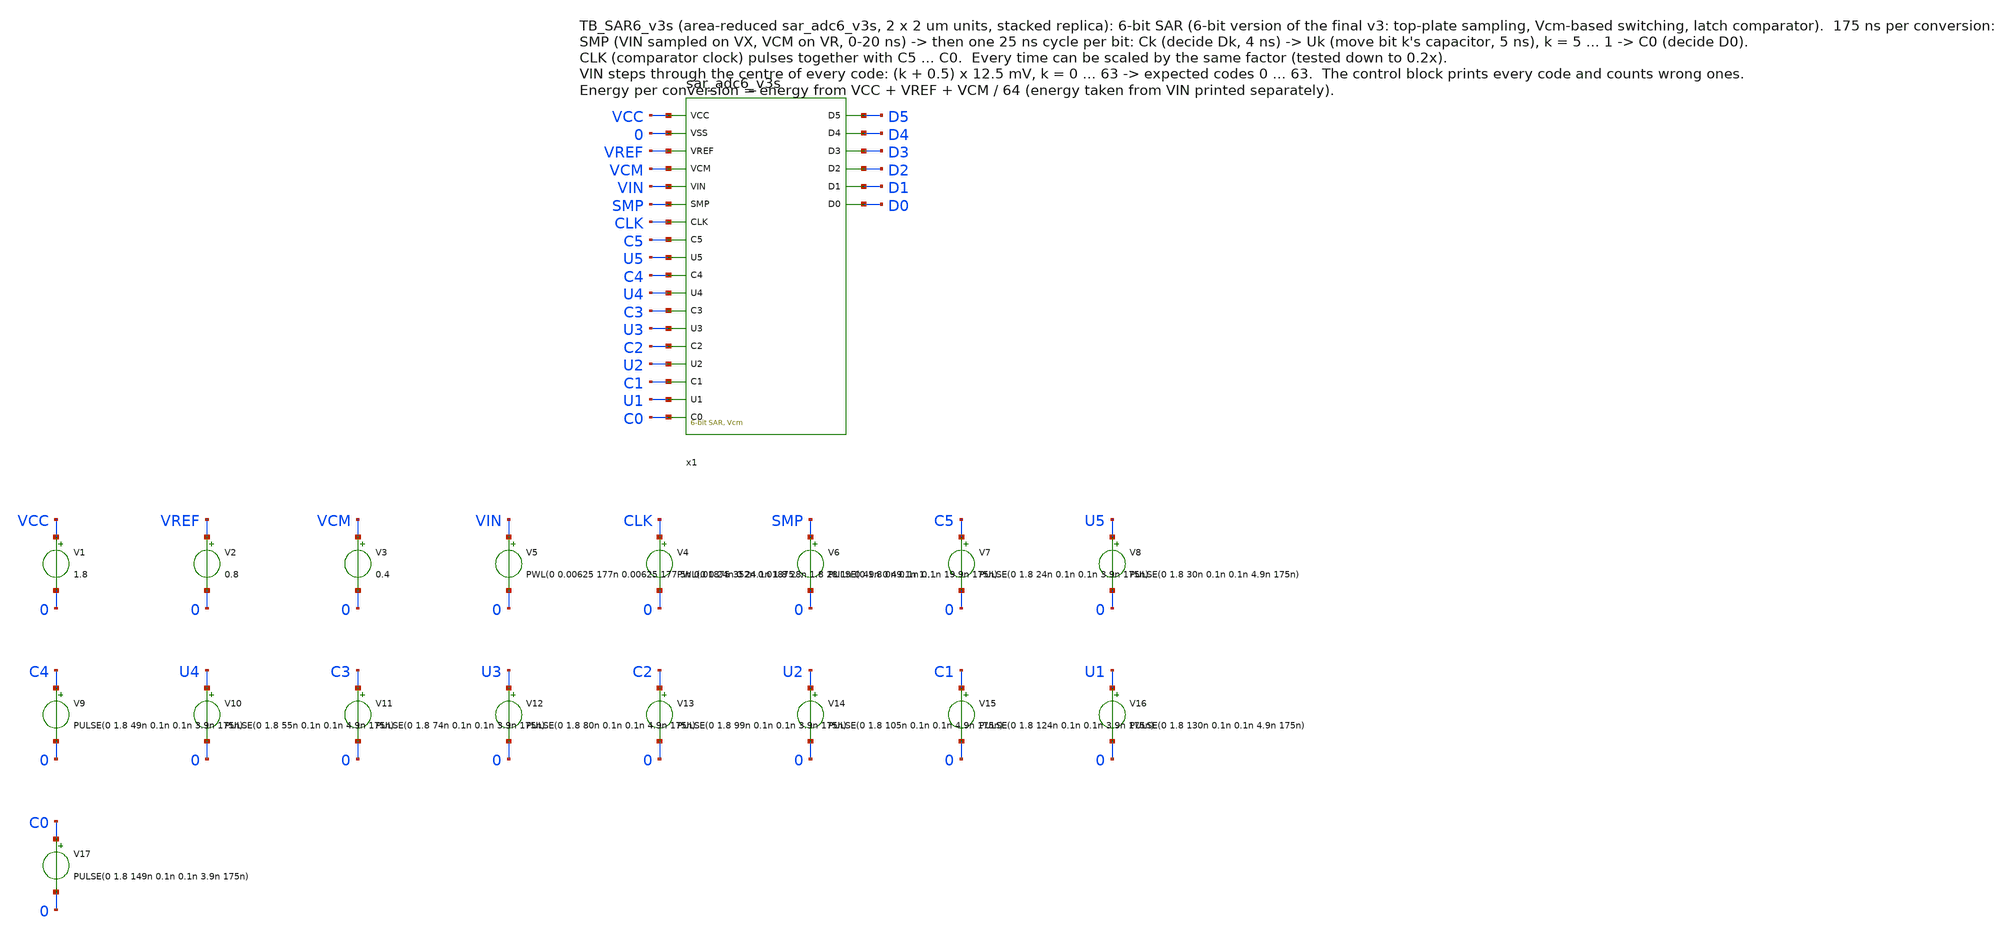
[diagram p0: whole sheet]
** sch_path: SAR_improved/TB_SAR6_v3s.sch
**.subckt TB_SAR6_v3s
x1 VCC 0 VREF VCM VIN SMP CLK C5 U5 C4 U4 C3 U3 C2 U2 C1 U1 C0 D5 D4 D3 D2 D1 D0 sar_adc6_v3s
V1 VCC 0 1.8
V2 VREF 0 0.8
V3 VCM 0 0.4
V5 VIN 0 PWL(0 0.00625 177n 0.00625 177.5n 0.01875 352n 0.01875 352.5n 0.03125 527n 0.03125 527.5n
+ 0.04375 702n 0.04375 702.5n 0.05625 877n 0.05625 877.5n 0.06875 1052n 0.06875 1052.5n 0.08125 1227n 0.08125
+ 1227.5n 0.09375 1402n 0.09375 1402.5n 0.10625 1577n 0.10625 1577.5n 0.11875 1752n 0.11875 1752.5n 0.13125
+ 1927n 0.13125 1927.5n 0.14375 2102n 0.14375 2102.5n 0.15625 2277n 0.15625 2277.5n 0.16875 2452n 0.16875
+ 2452.5n 0.18125 2627n 0.18125 2627.5n 0.19375 2802n 0.19375 2802.5n 0.20625 2977n 0.20625 2977.5n 0.21875
+ 3152n 0.21875 3152.5n 0.23125 3327n 0.23125 3327.5n 0.24375 3502n 0.24375 3502.5n 0.25625 3677n 0.25625
+ 3677.5n 0.26875 3852n 0.26875 3852.5n 0.28125 4027n 0.28125 4027.5n 0.29375 4202n 0.29375 4202.5n 0.30625
+ 4377n 0.30625 4377.5n 0.31875 4552n 0.31875 4552.5n 0.33125 4727n 0.33125 4727.5n 0.34375 4902n 0.34375
+ 4902.5n 0.35625 5077n 0.35625 5077.5n 0.36875 5252n 0.36875 5252.5n 0.38125 5427n 0.38125 5427.5n 0.39375
+ 5602n 0.39375 5602.5n 0.40625 5777n 0.40625 5777.5n 0.41875 5952n 0.41875 5952.5n 0.43125 6127n 0.43125
+ 6127.5n 0.44375 6302n 0.44375 6302.5n 0.45625 6477n 0.45625 6477.5n 0.46875 6652n 0.46875 6652.5n 0.48125
+ 6827n 0.48125 6827.5n 0.49375 7002n 0.49375 7002.5n 0.50625 7177n 0.50625 7177.5n 0.51875 7352n 0.51875
+ 7352.5n 0.53125 7527n 0.53125 7527.5n 0.54375 7702n 0.54375 7702.5n 0.55625 7877n 0.55625 7877.5n 0.56875
+ 8052n 0.56875 8052.5n 0.58125 8227n 0.58125 8227.5n 0.59375 8402n 0.59375 8402.5n 0.60625 8577n 0.60625
+ 8577.5n 0.61875 8752n 0.61875 8752.5n 0.63125 8927n 0.63125 8927.5n 0.64375 9102n 0.64375 9102.5n 0.65625
+ 9277n 0.65625 9277.5n 0.66875 9452n 0.66875 9452.5n 0.68125 9627n 0.68125 9627.5n 0.69375 9802n 0.69375
+ 9802.5n 0.70625 9977n 0.70625 9977.5n 0.71875 10152n 0.71875 10152.5n 0.73125 10327n 0.73125 10327.5n
+ 0.74375 10502n 0.74375 10502.5n 0.75625 10677n 0.75625 10677.5n 0.76875 10852n 0.76875 10852.5n 0.78125
+ 11027n 0.78125 11027.5n 0.79375)
V4 CLK 0 PWL(0 0 24n 0 24.1n 1.8 28n 1.8 28.1n 0 49n 0 49.1n 1.8 53n 1.8 53.1n 0 74n 0 74.1n 1.8 78n
+ 1.8 78.1n 0 99n 0 99.1n 1.8 103n 1.8 103.1n 0 124n 0 124.1n 1.8 128n 1.8 128.1n 0 149n 0 149.1n 1.8
+ 153n 1.8 153.1n 0 175n 0) r=0
V6 SMP 0 PULSE(0 1.8 0n 0.1n 0.1n 19.9n 175n)
V7 C5 0 PULSE(0 1.8 24n 0.1n 0.1n 3.9n 175n)
V8 U5 0 PULSE(0 1.8 30n 0.1n 0.1n 4.9n 175n)
V9 C4 0 PULSE(0 1.8 49n 0.1n 0.1n 3.9n 175n)
V10 U4 0 PULSE(0 1.8 55n 0.1n 0.1n 4.9n 175n)
V11 C3 0 PULSE(0 1.8 74n 0.1n 0.1n 3.9n 175n)
V12 U3 0 PULSE(0 1.8 80n 0.1n 0.1n 4.9n 175n)
V13 C2 0 PULSE(0 1.8 99n 0.1n 0.1n 3.9n 175n)
V14 U2 0 PULSE(0 1.8 105n 0.1n 0.1n 4.9n 175n)
V15 C1 0 PULSE(0 1.8 124n 0.1n 0.1n 3.9n 175n)
V16 U1 0 PULSE(0 1.8 130n 0.1n 0.1n 4.9n 175n)
V17 C0 0 PULSE(0 1.8 149n 0.1n 0.1n 3.9n 175n)
**** begin user architecture code

.lib /home/ttuser/pdk/sky130A/libs.tech/combined/sky130.lib.spice tt
.option method=gear reltol=1e-4
.control
save all
tran 0.05n 11200n
let code = 0*v(D0)
let code = code + 32*ceil((v(D5)-0.9)/10)
let code = code + 16*ceil((v(D4)-0.9)/10)
let code = code + 8*ceil((v(D3)-0.9)/10)
let code = code + 4*ceil((v(D2)-0.9)/10)
let code = code + 2*ceil((v(D1)-0.9)/10)
let code = code + 1*ceil((v(D0)-0.9)/10)
let nwrong = 0
let k = 0
while k < 64
  let tr = k*175e-9 + 165e-9
  meas tran ck find code at=$&tr
  print k ck
  if abs(ck - k) > 0.5
    let nwrong = nwrong + 1
  end
  let k = k + 1
end
print nwrong
let ptot = 1.8*(-i(V1)) + 0.8*(-i(V2)) + 0.4*(-i(V3))
let pin = v(VIN)*(-i(V5))
meas tran etot integ ptot from=0 to=11200n
meas tran ein integ pin from=0 to=11200n
let e_conv_pJ = etot/64*1e12
let e_from_vin_pJ = ein/64*1e12
let p_uW = etot/11200e-9*1e6
print e_conv_pJ p_uW e_from_vin_pJ
plot v(VIN) v(x1.VX) v(x1.VR)
plot v(SMP) v(CLK)+2 v(x1.COM)+4
plot v(x1.x2.BP5) v(x1.x2.BP4) v(x1.x2.BP3) v(x1.x2.BP2) v(x1.x2.BP1)
plot v(D5)+0 v(D4)+2 v(D3)+4 v(D2)+6 v(D1)+8 v(D0)+10
plot code
.endc

**** end user architecture code
**.ends
.end
